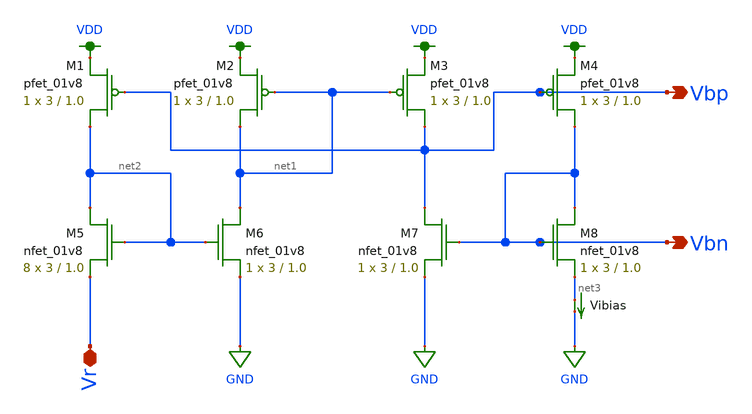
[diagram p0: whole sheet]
** sch_path: mini4/schem/ibias.sch
**.subckt ibias Vbn Vbp Vr
*.opin Vbn
*.opin Vbp
*.iopin Vr
XM1 net2 Vbp VDD VDD sky130_fd_pr__pfet_01v8 L=1.0 W=3 nf=1 ad='int((nf+1)/2) * W/nf * 0.29' as='int((nf+2)/2) * W/nf * 0.29'
+ pd='2*int((nf+1)/2) * (W/nf + 0.29)' ps='2*int((nf+2)/2) * (W/nf + 0.29)' nrd='0.29 / W' nrs='0.29 / W'
+ sa=0 sb=0 sd=0 mult=1 m=1
XM2 net1 net1 VDD VDD sky130_fd_pr__pfet_01v8 L=1.0 W=3 nf=1 ad='int((nf+1)/2) * W/nf * 0.29' as='int((nf+2)/2) * W/nf * 0.29'
+ pd='2*int((nf+1)/2) * (W/nf + 0.29)' ps='2*int((nf+2)/2) * (W/nf + 0.29)' nrd='0.29 / W' nrs='0.29 / W'
+ sa=0 sb=0 sd=0 mult=1 m=1
XM3 Vbp net1 VDD VDD sky130_fd_pr__pfet_01v8 L=1.0 W=3 nf=1 ad='int((nf+1)/2) * W/nf * 0.29' as='int((nf+2)/2) * W/nf * 0.29'
+ pd='2*int((nf+1)/2) * (W/nf + 0.29)' ps='2*int((nf+2)/2) * (W/nf + 0.29)' nrd='0.29 / W' nrs='0.29 / W'
+ sa=0 sb=0 sd=0 mult=1 m=1
XM4 Vbn Vbp VDD VDD sky130_fd_pr__pfet_01v8 L=1.0 W=3 nf=1 ad='int((nf+1)/2) * W/nf * 0.29' as='int((nf+2)/2) * W/nf * 0.29'
+ pd='2*int((nf+1)/2) * (W/nf + 0.29)' ps='2*int((nf+2)/2) * (W/nf + 0.29)' nrd='0.29 / W' nrs='0.29 / W'
+ sa=0 sb=0 sd=0 mult=1 m=1
XM5 net2 net2 Vr GND sky130_fd_pr__nfet_01v8 L=1.0 W=3 nf=1 ad='int((nf+1)/2) * W/nf * 0.29' as='int((nf+2)/2) * W/nf * 0.29'
+ pd='2*int((nf+1)/2) * (W/nf + 0.29)' ps='2*int((nf+2)/2) * (W/nf + 0.29)' nrd='0.29 / W' nrs='0.29 / W'
+ sa=0 sb=0 sd=0 mult=8 m=8
XM6 net1 net2 GND GND sky130_fd_pr__nfet_01v8 L=1.0 W=3 nf=1 ad='int((nf+1)/2) * W/nf * 0.29' as='int((nf+2)/2) * W/nf * 0.29'
+ pd='2*int((nf+1)/2) * (W/nf + 0.29)' ps='2*int((nf+2)/2) * (W/nf + 0.29)' nrd='0.29 / W' nrs='0.29 / W'
+ sa=0 sb=0 sd=0 mult=1 m=1
XM7 Vbp Vbn GND GND sky130_fd_pr__nfet_01v8 L=1.0 W=3 nf=1 ad='int((nf+1)/2) * W/nf * 0.29' as='int((nf+2)/2) * W/nf * 0.29'
+ pd='2*int((nf+1)/2) * (W/nf + 0.29)' ps='2*int((nf+2)/2) * (W/nf + 0.29)' nrd='0.29 / W' nrs='0.29 / W'
+ sa=0 sb=0 sd=0 mult=1 m=1
XM8 Vbn Vbn net3 GND sky130_fd_pr__nfet_01v8 L=1.0 W=3 nf=1 ad='int((nf+1)/2) * W/nf * 0.29' as='int((nf+2)/2) * W/nf * 0.29'
+ pd='2*int((nf+1)/2) * (W/nf + 0.29)' ps='2*int((nf+2)/2) * (W/nf + 0.29)' nrd='0.29 / W' nrs='0.29 / W'
+ sa=0 sb=0 sd=0 mult=1 m=1
Vibias net3 GND 0
.save i(vibias)
**.ends
.GLOBAL VDD
.GLOBAL GND
.end
